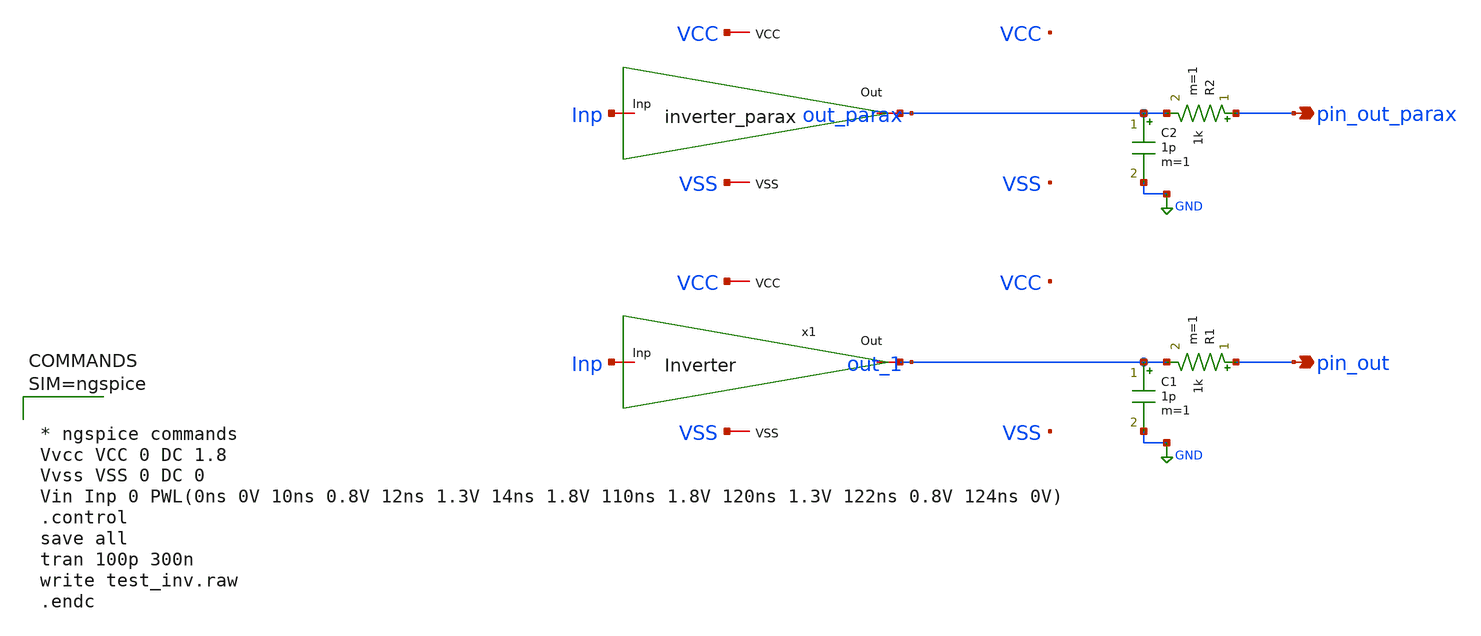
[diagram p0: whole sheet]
** sch_path: xschem/test_inv.sch
**.subckt test_inv pin_out pin_out_parax
*.opin pin_out
*.opin pin_out_parax
x1 VCC out_1 Inp VSS Inverter
R1 pin_out out_1 1k m=1
C1 out_1 GND 1p m=1
x1 VCC out_parax Inp VSS inverter_parax
R2 pin_out_parax out_parax 1k m=1
C2 out_parax GND 1p m=1
**** begin user architecture code

** opencircuitdesign pdks install
.lib $::SKYWATER_MODELS/sky130.lib.spice tt




* ngspice commands
Vvcc VCC 0 DC 1.8
Vvss VSS 0 DC 0
Vin Inp 0 PWL(0ns 0V 10ns 0.8V 12ns 1.3V 14ns 1.8V 110ns 1.8V 120ns 1.3V 122ns 0.8V 124ns 0V)
.control
save all
tran 100p 300n
write test_inv.raw
.endc



**** end user architecture code
**.ends

* expanding   symbol:  Inverter.sym # of pins=4
** sym_path: xschem/Inverter.sym
** sch_path: xschem/Inverter.sch
.subckt Inverter VCC Out Inp VSS
*.iopin Inp
*.iopin VSS
*.iopin Out
*.iopin VCC
XM2 Out Inp VCC VCC sky130_fd_pr__pfet_01v8 L=0.15 W=2 nf=1 ad='int((1 + 1)/2) * 2 / 1 * 0.29' as='int((1 + 2)/2) * 2 / 1 * 0.29'
+ pd='2*int((1 + 1)/2) * (2 / 1 + 0.29)' ps='2*int((1 + 2)/2) * (2 / 1 + 0.29)' nrd='0.29 / 2 ' nrs='0.29 / 2 '
+ sa=0 sb=0 sd=0 mult=1 m=1
XM3 Out Inp VSS VSS sky130_fd_pr__nfet_01v8 L=0.15 W=1 nf=1 ad='int((1 + 1)/2) * 1 / 1 * 0.29' as='int((1 + 2)/2) * 1 / 1 * 0.29'
+ pd='2*int((1 + 1)/2) * (1 / 1 + 0.29)' ps='2*int((1 + 2)/2) * (1 / 1 + 0.29)' nrd='0.29 / 1 ' nrs='0.29 / 1 '
+ sa=0 sb=0 sd=0 mult=1 m=1
.ends


* expanding   symbol:  inverter_parax.sym # of pins=4
** sym_path: xschem/Inverter.sym
.include [file normalize ../mag/Inverter.sim.spice]
.GLOBAL GND
.end
